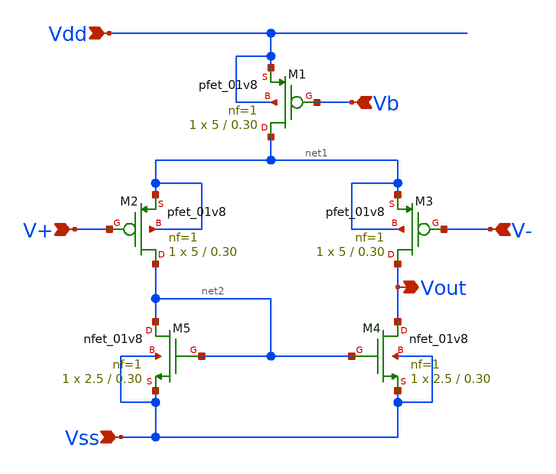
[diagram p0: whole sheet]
** sch_path: Bandgap/ota.sch
**.subckt ota Vdd Vout V+ V- Vss Vb
*.ipin Vdd
*.opin Vout
*.ipin V+
*.ipin V-
*.ipin Vss
*.ipin Vb
XM1 net1 Vb Vdd Vdd sky130_fd_pr__pfet_01v8 L=0.30 W=5 nf=1 ad='int((1 + 1)/2) * 5 / 1 * 0.29' as='int((1 + 2)/2) * 5 / 1 * 0.29'
+ pd='2*int((1 + 1)/2) * (5 / 1 + 0.29)' ps='2*int((1 + 2)/2) * (5 / 1 + 0.29)' nrd='0.29 / 5 ' nrs='0.29 / 5 '
+ sa=0 sb=0 sd=0 mult=1 m=1
XM2 net2 V+ net1 net1 sky130_fd_pr__pfet_01v8 L=0.30 W=5 nf=1 ad='int((1 + 1)/2) * 5 / 1 * 0.29' as='int((1 + 2)/2) * 5 / 1 * 0.29'
+ pd='2*int((1 + 1)/2) * (5 / 1 + 0.29)' ps='2*int((1 + 2)/2) * (5 / 1 + 0.29)' nrd='0.29 / 5 ' nrs='0.29 / 5 '
+ sa=0 sb=0 sd=0 mult=1 m=1
XM3 Vout V- net1 net1 sky130_fd_pr__pfet_01v8 L=0.30 W=5 nf=1 ad='int((1 + 1)/2) * 5 / 1 * 0.29' as='int((1 + 2)/2) * 5 / 1 * 0.29'
+ pd='2*int((1 + 1)/2) * (5 / 1 + 0.29)' ps='2*int((1 + 2)/2) * (5 / 1 + 0.29)' nrd='0.29 / 5 ' nrs='0.29 / 5 '
+ sa=0 sb=0 sd=0 mult=1 m=1
XM4 Vout net2 Vss Vss sky130_fd_pr__nfet_01v8 L=0.30 W=2.5 nf=1 ad='int((1 + 1)/2) * 2.5 / 1 * 0.29'
+ as='int((1 + 2)/2) * 2.5 / 1 * 0.29' pd='2*int((1 + 1)/2) * (2.5 / 1 + 0.29)' ps='2*int((1 + 2)/2) * (2.5 / 1 + 0.29)'
+ nrd='0.29 / 2.5 ' nrs='0.29 / 2.5 ' sa=0 sb=0 sd=0 mult=1 m=1
XM5 net2 net2 Vss Vss sky130_fd_pr__nfet_01v8 L=0.30 W=2.5 nf=1 ad='int((1 + 1)/2) * 2.5 / 1 * 0.29'
+ as='int((1 + 2)/2) * 2.5 / 1 * 0.29' pd='2*int((1 + 1)/2) * (2.5 / 1 + 0.29)' ps='2*int((1 + 2)/2) * (2.5 / 1 + 0.29)'
+ nrd='0.29 / 2.5 ' nrs='0.29 / 2.5 ' sa=0 sb=0 sd=0 mult=1 m=1
**.ends
.end
